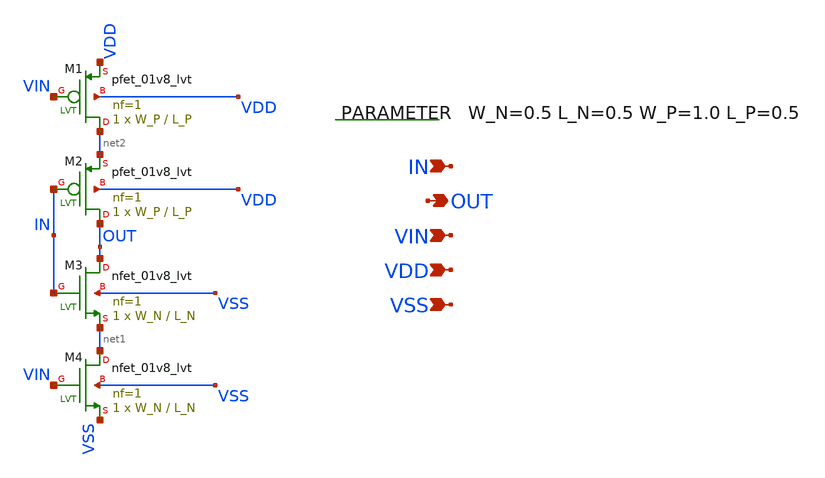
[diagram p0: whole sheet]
** sch_path: xschem/epc_delay.sch
**.subckt epc_delay VDD VIN IN VSS OUT
*.ipin VDD
*.ipin VIN
*.ipin IN
*.ipin VSS
*.opin OUT
.param W_N=0.5 L_N=0.5 W_P=1.0 L_P=0.5
XM1 net2 VIN VDD VDD sky130_fd_pr__pfet_01v8_lvt L=L_P W=W_P nf=1 ad='int((nf+1)/2) * W/nf * 0.29' as='int((nf+2)/2) * W/nf * 0.29'
+ pd='2*int((nf+1)/2) * (W/nf + 0.29)' ps='2*int((nf+2)/2) * (W/nf + 0.29)' nrd='0.29 / W' nrs='0.29 / W'
+ sa=0 sb=0 sd=0 mult=1 m=1
XM2 OUT IN net2 VDD sky130_fd_pr__pfet_01v8_lvt L=L_P W=W_P nf=1 ad='int((nf+1)/2) * W/nf * 0.29' as='int((nf+2)/2) * W/nf * 0.29'
+ pd='2*int((nf+1)/2) * (W/nf + 0.29)' ps='2*int((nf+2)/2) * (W/nf + 0.29)' nrd='0.29 / W' nrs='0.29 / W'
+ sa=0 sb=0 sd=0 mult=1 m=1
XM3 OUT IN net1 VSS sky130_fd_pr__nfet_01v8_lvt L=L_N W=W_N nf=1 ad='int((nf+1)/2) * W/nf * 0.29' as='int((nf+2)/2) * W/nf * 0.29'
+ pd='2*int((nf+1)/2) * (W/nf + 0.29)' ps='2*int((nf+2)/2) * (W/nf + 0.29)' nrd='0.29 / W' nrs='0.29 / W'
+ sa=0 sb=0 sd=0 mult=1 m=1
XM4 net1 VIN VSS VSS sky130_fd_pr__nfet_01v8_lvt L=L_N W=W_N nf=1 ad='int((nf+1)/2) * W/nf * 0.29' as='int((nf+2)/2) * W/nf * 0.29'
+ pd='2*int((nf+1)/2) * (W/nf + 0.29)' ps='2*int((nf+2)/2) * (W/nf + 0.29)' nrd='0.29 / W' nrs='0.29 / W'
+ sa=0 sb=0 sd=0 mult=1 m=1
**.ends
.end
